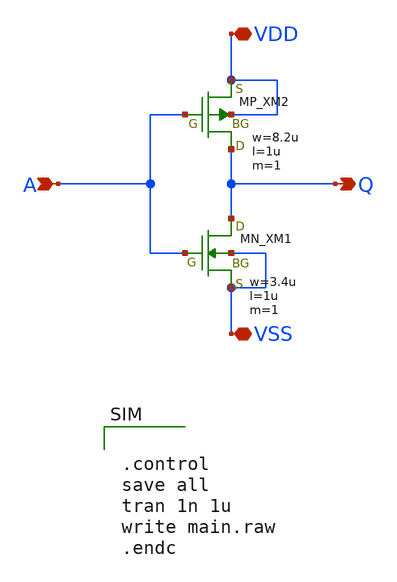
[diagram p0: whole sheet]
** sch_path: ytr0_inverter.sch
**.subckt ytr0_inverter A Q VDD VSS
*.ipin A
*.opin Q
*.iopin VDD
*.iopin VSS
XXM1 Q A VSS VSS NMOS w=3.4u l=1u nrd=0 nrs=0 m=1
XXM2 Q A VDD VDD PMOS w=8.2u l=1u nrd=0 nrs=0 m=1
**** begin user architecture code
 .include $::LIB/ip62_models


.control
save all
tran 1n 1u
write main.raw
.endc


**** end user architecture code
**.ends
.end
